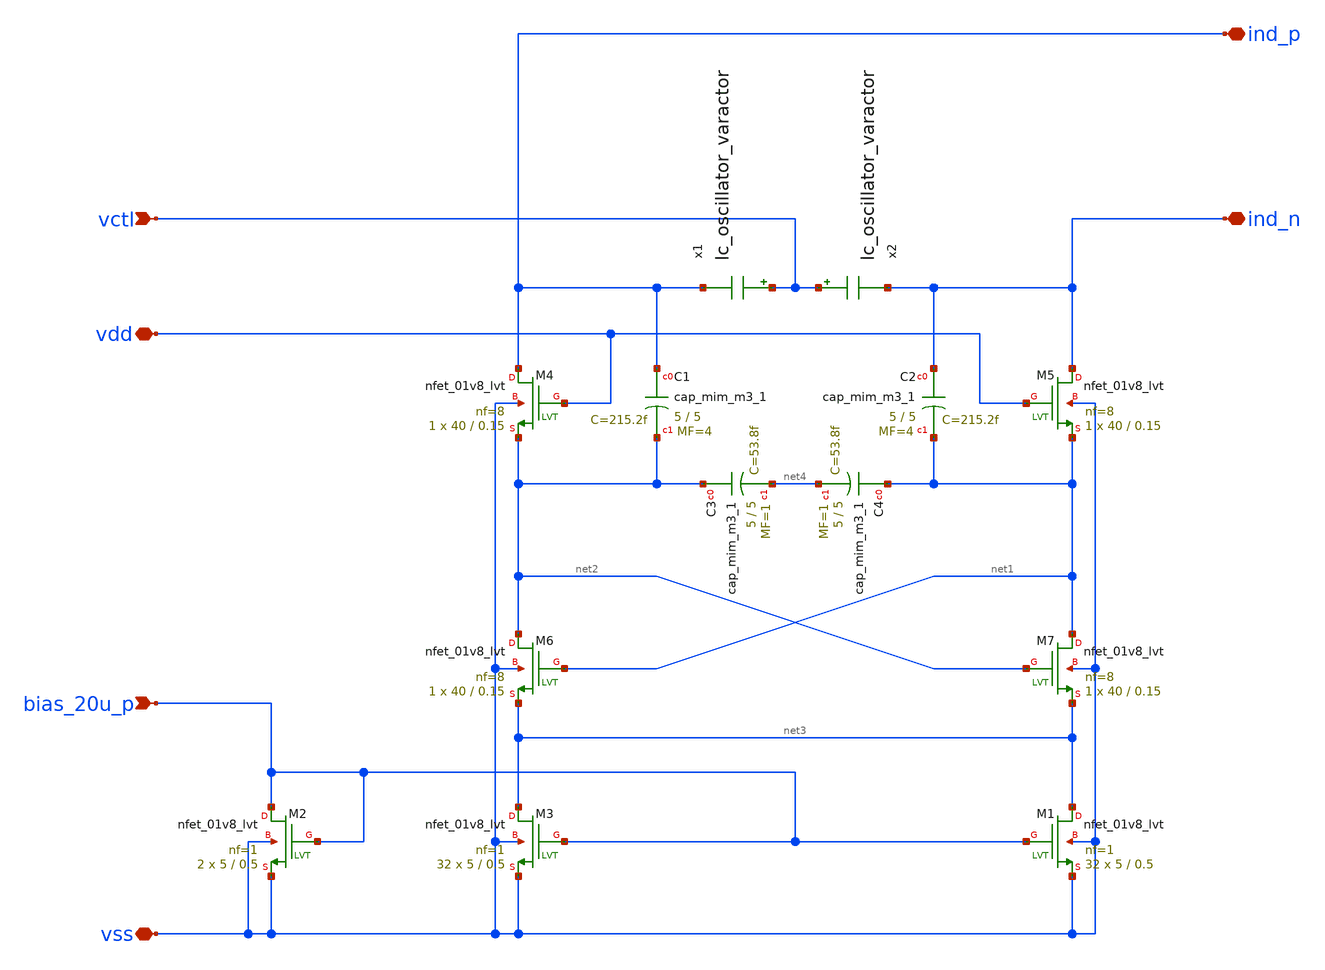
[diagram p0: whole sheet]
** sch_path: design/lc_oscillator_core/lc_oscillator_core.sch
**.subckt lc_oscillator_core vctl vss bias_20u_p vdd ind_n ind_p
*.ipin vctl
*.iopin vss
*.ipin bias_20u_p
*.iopin vdd
*.iopin ind_n
*.iopin ind_p
XM2 bias_20u_p bias_20u_p vss vss sky130_fd_pr__nfet_01v8_lvt L=0.5 W=5 nf=1 ad='int((nf+1)/2) * W/nf * 0.29'
+ as='int((nf+2)/2) * W/nf * 0.29' pd='2*int((nf+1)/2) * (W/nf + 0.29)' ps='2*int((nf+2)/2) * (W/nf + 0.29)'
+ nrd='0.29 / W' nrs='0.29 / W' sa=0 sb=0 sd=0 mult=2 m=2
XM1 net3 bias_20u_p vss vss sky130_fd_pr__nfet_01v8_lvt L=0.5 W=5 nf=1 ad='int((nf+1)/2) * W/nf * 0.29'
+ as='int((nf+2)/2) * W/nf * 0.29' pd='2*int((nf+1)/2) * (W/nf + 0.29)' ps='2*int((nf+2)/2) * (W/nf + 0.29)'
+ nrd='0.29 / W' nrs='0.29 / W' sa=0 sb=0 sd=0 mult=32 m=32
XM3 net3 bias_20u_p vss vss sky130_fd_pr__nfet_01v8_lvt L=0.5 W=5 nf=1 ad='int((nf+1)/2) * W/nf * 0.29'
+ as='int((nf+2)/2) * W/nf * 0.29' pd='2*int((nf+1)/2) * (W/nf + 0.29)' ps='2*int((nf+2)/2) * (W/nf + 0.29)'
+ nrd='0.29 / W' nrs='0.29 / W' sa=0 sb=0 sd=0 mult=32 m=32
XC1 ind_p net2 sky130_fd_pr__cap_mim_m3_1 W=5 L=5 MF=4 m=4
XC2 ind_n net1 sky130_fd_pr__cap_mim_m3_1 W=5 L=5 MF=4 m=4
XC3 net2 net4 sky130_fd_pr__cap_mim_m3_1 W=5 L=5 MF=1 m=1
XC4 net1 net4 sky130_fd_pr__cap_mim_m3_1 W=5 L=5 MF=1 m=1
XM4 ind_p vdd net2 vss sky130_fd_pr__nfet_01v8_lvt L=0.15 W=40 nf=8 ad='int((nf+1)/2) * W/nf * 0.29'
+ as='int((nf+2)/2) * W/nf * 0.29' pd='2*int((nf+1)/2) * (W/nf + 0.29)' ps='2*int((nf+2)/2) * (W/nf + 0.29)'
+ nrd='0.29 / W' nrs='0.29 / W' sa=0 sb=0 sd=0 mult=1 m=1
XM5 ind_n vdd net1 vss sky130_fd_pr__nfet_01v8_lvt L=0.15 W=40 nf=8 ad='int((nf+1)/2) * W/nf * 0.29'
+ as='int((nf+2)/2) * W/nf * 0.29' pd='2*int((nf+1)/2) * (W/nf + 0.29)' ps='2*int((nf+2)/2) * (W/nf + 0.29)'
+ nrd='0.29 / W' nrs='0.29 / W' sa=0 sb=0 sd=0 mult=1 m=1
XM6 net2 net1 net3 vss sky130_fd_pr__nfet_01v8_lvt L=0.15 W=40 nf=8 ad='int((nf+1)/2) * W/nf * 0.29'
+ as='int((nf+2)/2) * W/nf * 0.29' pd='2*int((nf+1)/2) * (W/nf + 0.29)' ps='2*int((nf+2)/2) * (W/nf + 0.29)'
+ nrd='0.29 / W' nrs='0.29 / W' sa=0 sb=0 sd=0 mult=1 m=1
XM7 net1 net2 net3 vss sky130_fd_pr__nfet_01v8_lvt L=0.15 W=40 nf=8 ad='int((nf+1)/2) * W/nf * 0.29'
+ as='int((nf+2)/2) * W/nf * 0.29' pd='2*int((nf+1)/2) * (W/nf + 0.29)' ps='2*int((nf+2)/2) * (W/nf + 0.29)'
+ nrd='0.29 / W' nrs='0.29 / W' sa=0 sb=0 sd=0 mult=1 m=1
x1 vctl ind_p lc_oscillator_varactor
x2 vctl ind_n lc_oscillator_varactor
**.ends

* expanding   symbol:  lc_oscillator_varactor/lc_oscillator_varactor.sym # of pins=2
** sym_path: design/lc_oscillator_varactor/lc_oscillator_varactor.sym
** sch_path: design/lc_oscillator_varactor/lc_oscillator_varactor.sch
.subckt lc_oscillator_varactor p m
*.iopin p
*.iopin m
XM1 p m p p sky130_fd_pr__pfet_01v8 L=4 W=4 nf=1 ad='int((nf+1)/2) * W/nf * 0.29' as='int((nf+2)/2) * W/nf * 0.29'
+ pd='2*int((nf+1)/2) * (W/nf + 0.29)' ps='2*int((nf+2)/2) * (W/nf + 0.29)' nrd='0.29 / W' nrs='0.29 / W'
+ sa=0 sb=0 sd=0 mult=1 m=1
.ends

.end
